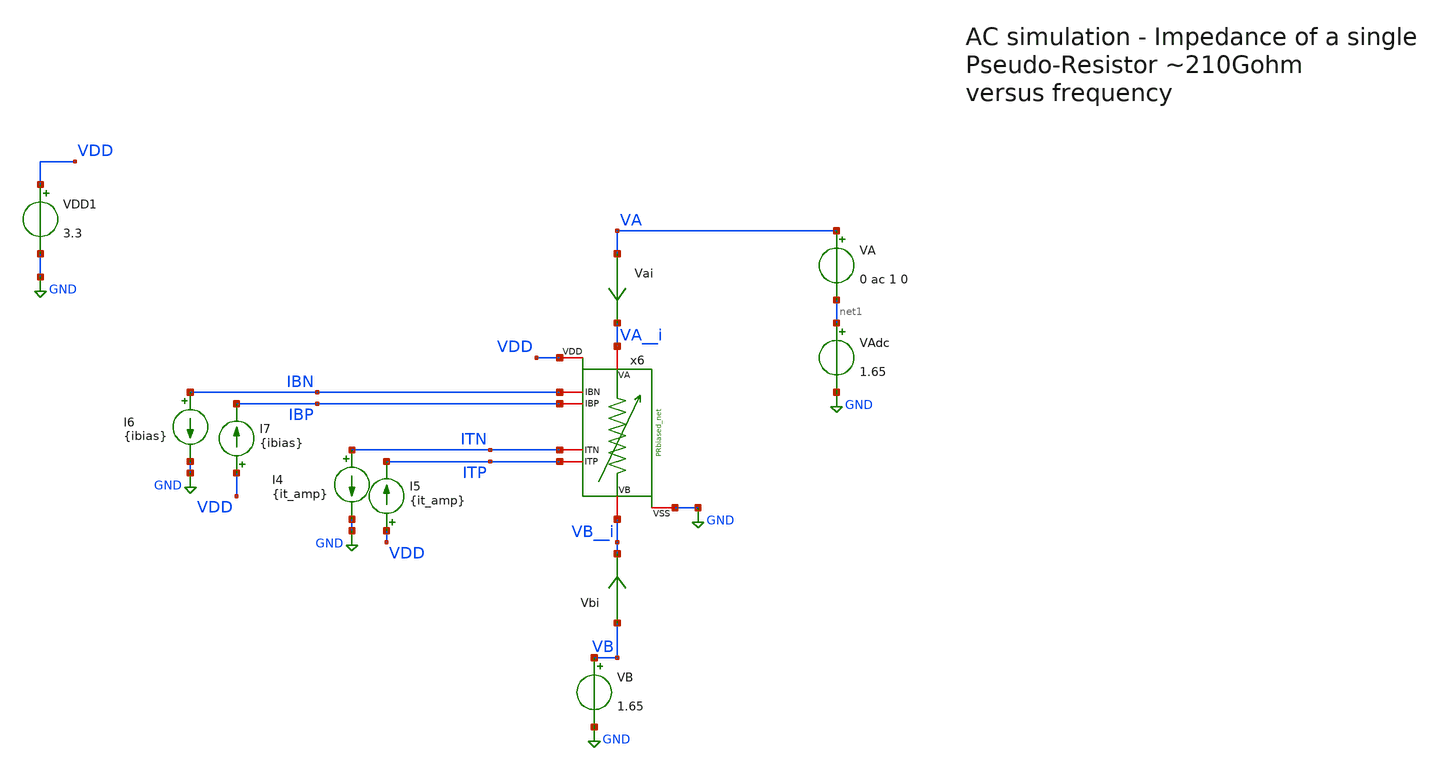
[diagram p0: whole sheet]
** sch_path: TIA_Filter/PseudoResistor/TB_PR_single_ac.sch
**.subckt TB_PR_single_ac
VDD1 VDD GND 3.3
VA VA net1 0 ac 1 0
VB VB GND 1.65
VAdc net1 GND 1.65
x6 VA__i VB__i IBN IBP ITN ITP VDD GND PRbiased_net
I4 ITN GND {it_amp}
I5 VDD ITP {it_amp}
I6 IBN GND {ibias}
I7 VDD IBP {ibias}
Vai VA VA__i 0
.save i(vai)
Vbi VB VB__i 0
.save i(vbi)
**** begin user architecture code


.option savecurrents
.option gmin=1e-24

.param ibias = 1p
.param it_amp = 2p

.nodeset all=1.65

.control

  op
  let imped = 0
  save imped
  remzerovec
  write TB_PR_single_ac.raw
  set appendwrite

  set temp = 27
  ac dec 100 1m 1e7
  let imped = -V(va)/i(va)
  save imped
  remzerovec
  write TB_PR_single_ac.raw
  *wrdata
+ /home/gmaranhao/Desktop/Bracolin/TIA_Filter/PseudoResistor/plots/data_DC/PR_single_AC_tt.txt I(VA) imped

.endc
.save all



.include $::180MCU_MODELS/design.ngspice
.lib $::180MCU_MODELS/sm141064.ngspice typical

*.param sw_stat_mismatch=1
*.param sw_stat_global=1


**** end user architecture code
**.ends
.GLOBAL GND
.end
